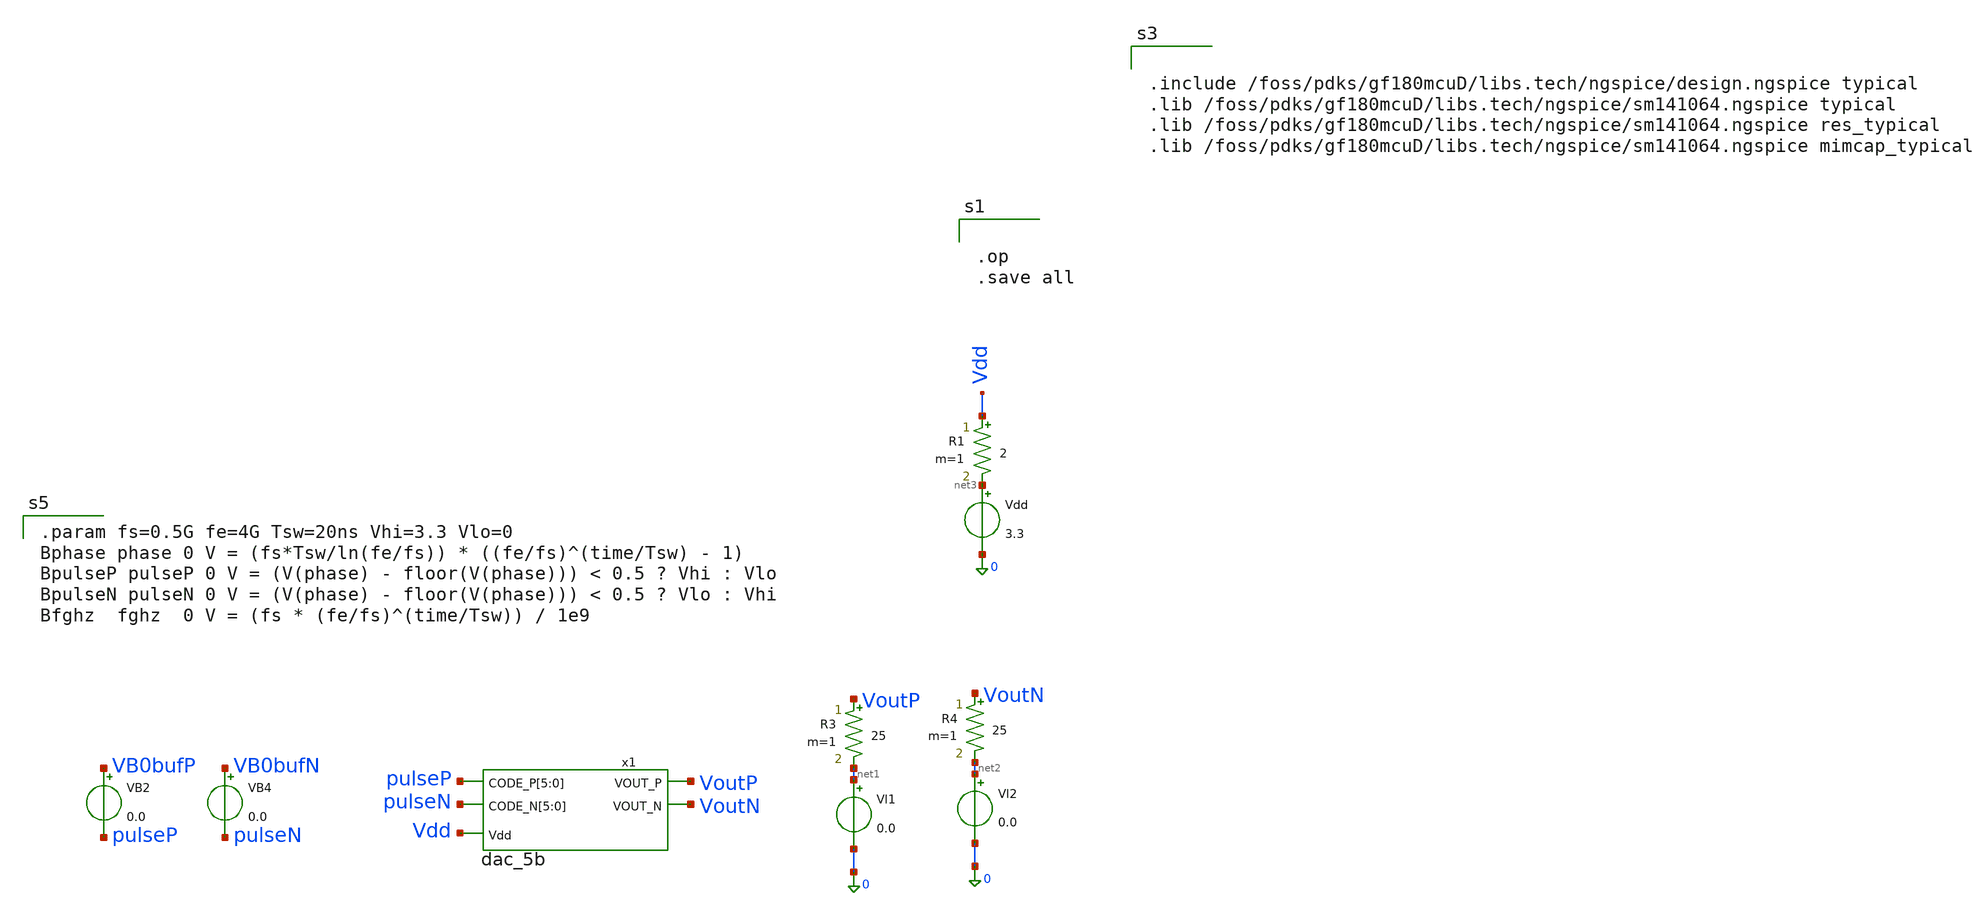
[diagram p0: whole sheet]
** sch_path: blocks/dac/test/test_dac_fsweep_5b.sch
**.subckt test_dac_fsweep_5b
Vdd net3 0 3.3
.save i(vdd)
R3 VoutP net1 25 m=1
R4 VoutN net2 25 m=1
Vl1 net1 0 0.0
.save i(vl1)
Vl2 net2 0 0.0
.save i(vl2)
VB2 VB0bufP pulseP 0.0
.save i(vb2)
VB4 VB0bufN pulseN 0.0
.save i(vb4)
R1 Vdd net3 2 m=1
x1 Vdd VoutP pulseP pulseP pulseP pulseP pulseP pulseP VoutN pulseN pulseN pulseN pulseN pulseN
+ pulseN dac_5b
**** begin user architecture code



.save all
.control

tran 1p 10ns
plot ClkP+5 ClkN+5 VB3bufP-5 VB3bufN-5 x1.Vg1P-10 x1.Vg1N-10 x2.Vg1P-15 x2.Vg1N-15

plot i(v.x1.VB3P)-i(v.x1.VB3N) i(v.x1.VU0P)-i(v.x1.VU0N) i(v.x1.VB4P)-i(v.x1.VB4N)
+ i(v.x1.VB2P)-i(v.x1.VB2N) i(v.x1.VB1P)-i(v.x1.VB1N)

let diff = i(Vl1)-i(Vl2)

let imax = 630E-6
let imin = -630E-6
plot pulseP {diff/{imax}}*5 fghz

plot VoutP VoutN pulseP+5 pulseN+5

plot i(Vl1)-i(Vl2) imax imin fghz*100E-6
plot i(Vdd)

plot i(v.x1.VU0P) i(v.x1.VU0N)
plot i(v.x1.VU0P)-i(v.x1.VU0N)

* plot i(VoutB3P)+100E-6 i(VoutB3N)+100E-6 i(VoutB3P)-i(VoutB3N) i(VoutB3N)+i(VoutB3P)
*+ i(v.x1.Vcrr1)-200E-6 i(v.x1.Vcrr2)-200E-6
* plot i(Vl1) VB1in/5E4+200E-6 VU0in/5E4+200E-6
.endc





.op
.save all



.param fs=0.5G fe=4G Tsw=20ns Vhi=3.3 Vlo=0
Bphase phase 0 V = (fs*Tsw/ln(fe/fs)) * ((fe/fs)^(time/Tsw) - 1)
BpulseP pulseP 0 V = (V(phase) - floor(V(phase))) < 0.5 ? Vhi : Vlo
BpulseN pulseN 0 V = (V(phase) - floor(V(phase))) < 0.5 ? Vlo : Vhi
Bfghz  fghz  0 V = (fs * (fe/fs)^(time/Tsw)) / 1e9





.include /foss/pdks/gf180mcuD/libs.tech/ngspice/design.ngspice typical
.lib /foss/pdks/gf180mcuD/libs.tech/ngspice/sm141064.ngspice typical
.lib /foss/pdks/gf180mcuD/libs.tech/ngspice/sm141064.ngspice res_typical
.lib /foss/pdks/gf180mcuD/libs.tech/ngspice/sm141064.ngspice mimcap_typical


**** end user architecture code
**.ends
.end
